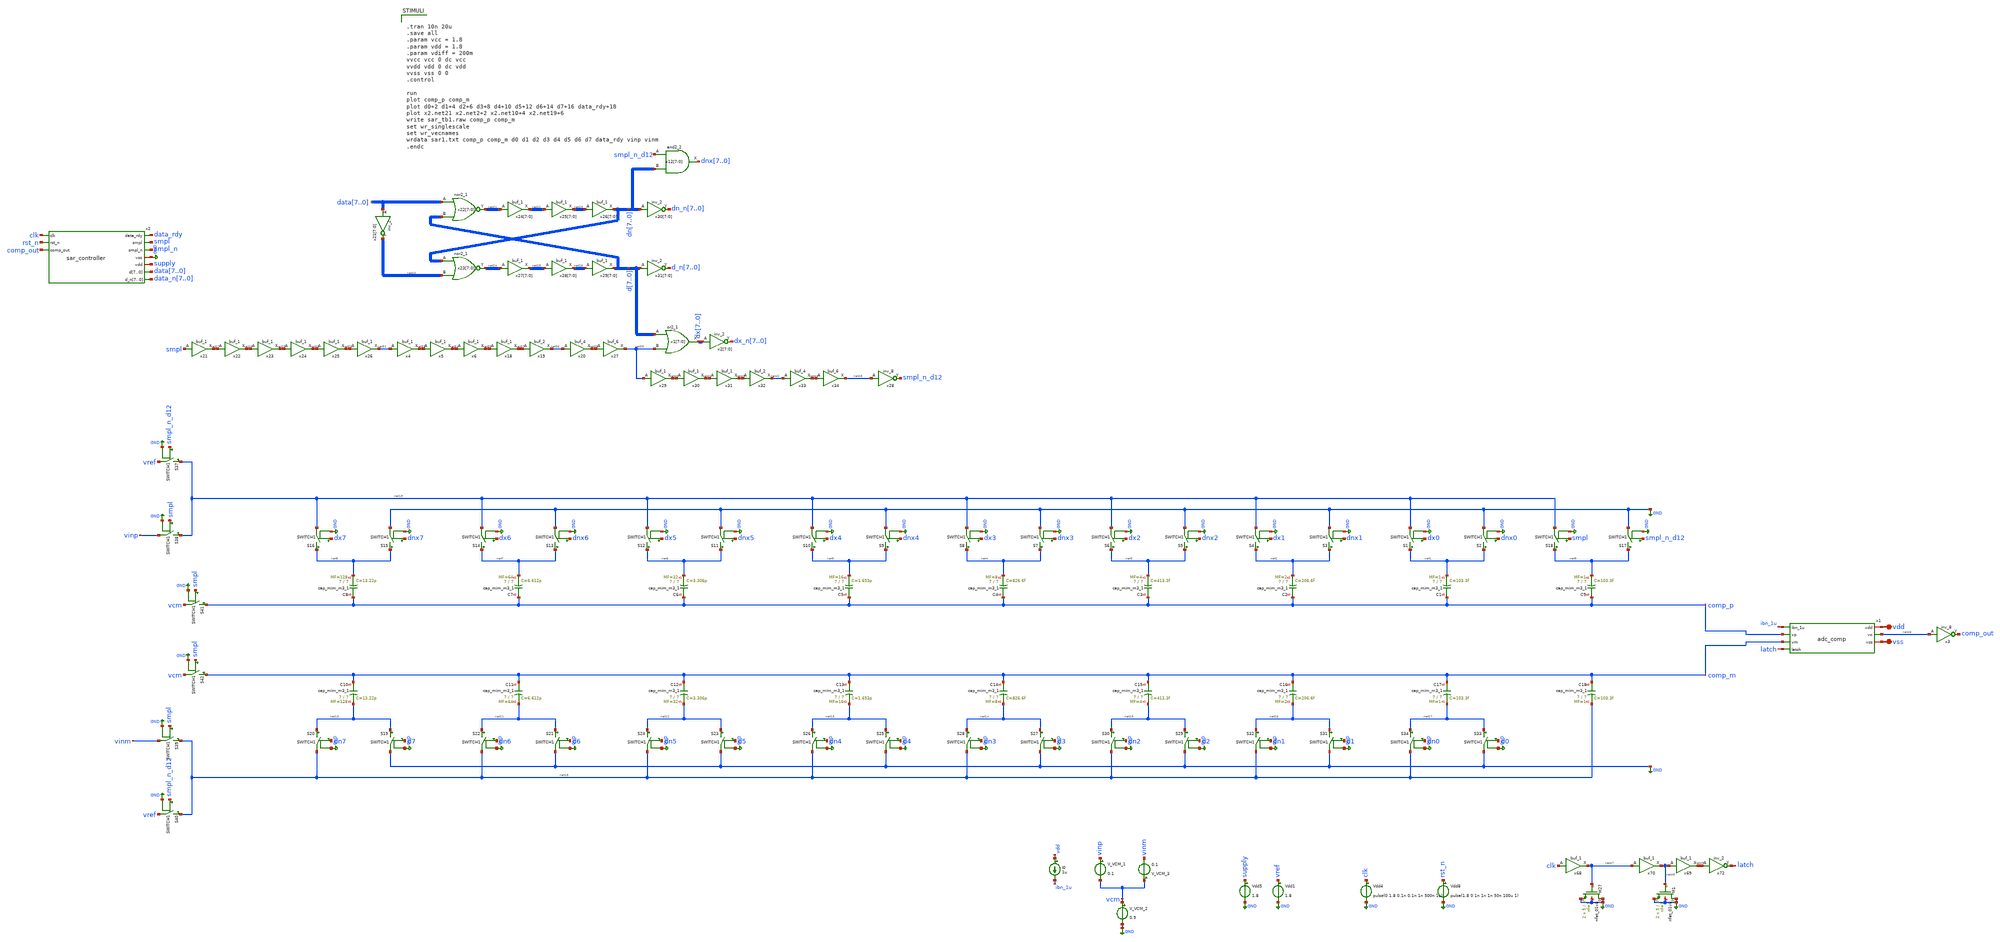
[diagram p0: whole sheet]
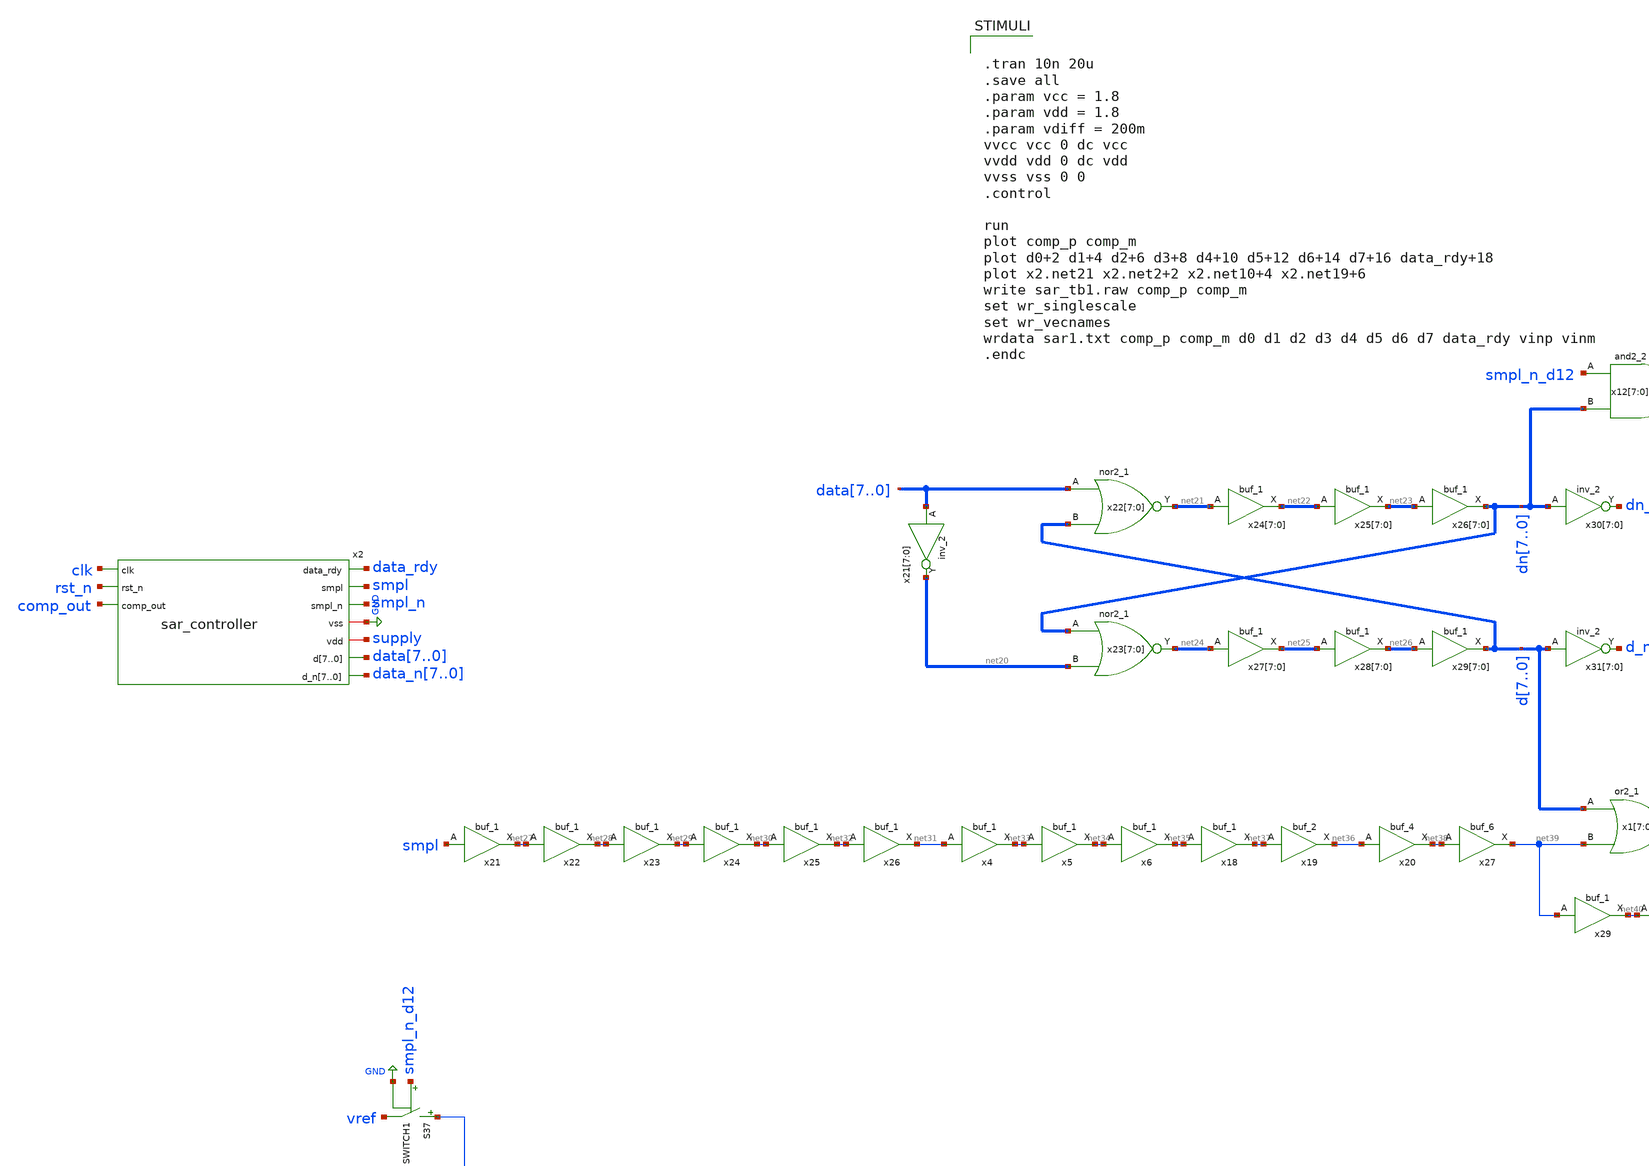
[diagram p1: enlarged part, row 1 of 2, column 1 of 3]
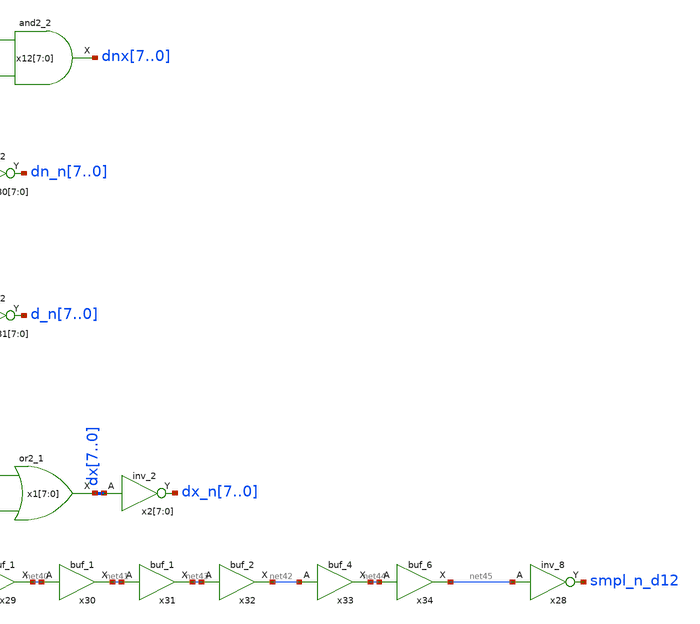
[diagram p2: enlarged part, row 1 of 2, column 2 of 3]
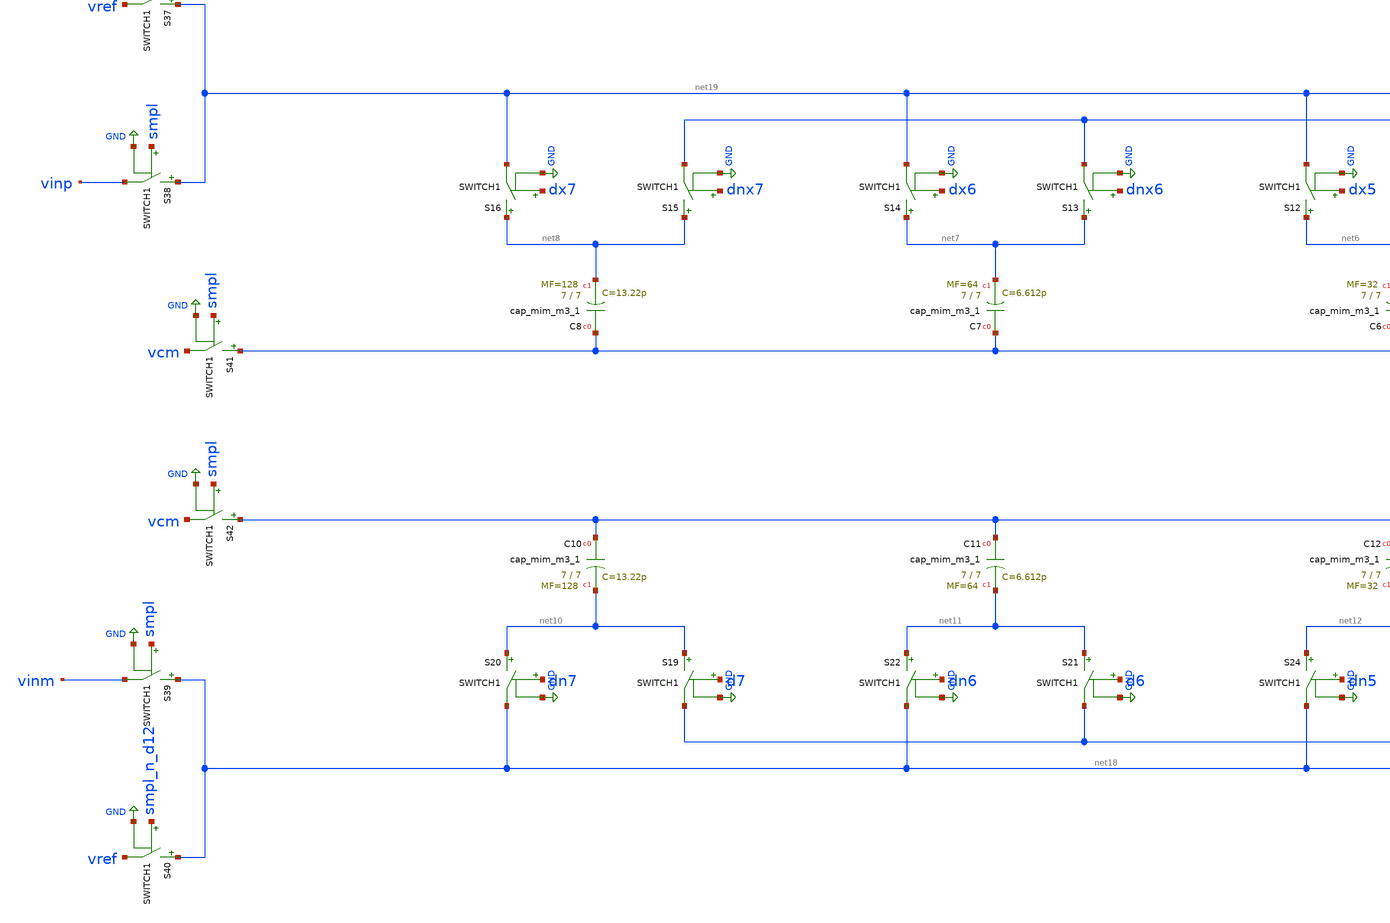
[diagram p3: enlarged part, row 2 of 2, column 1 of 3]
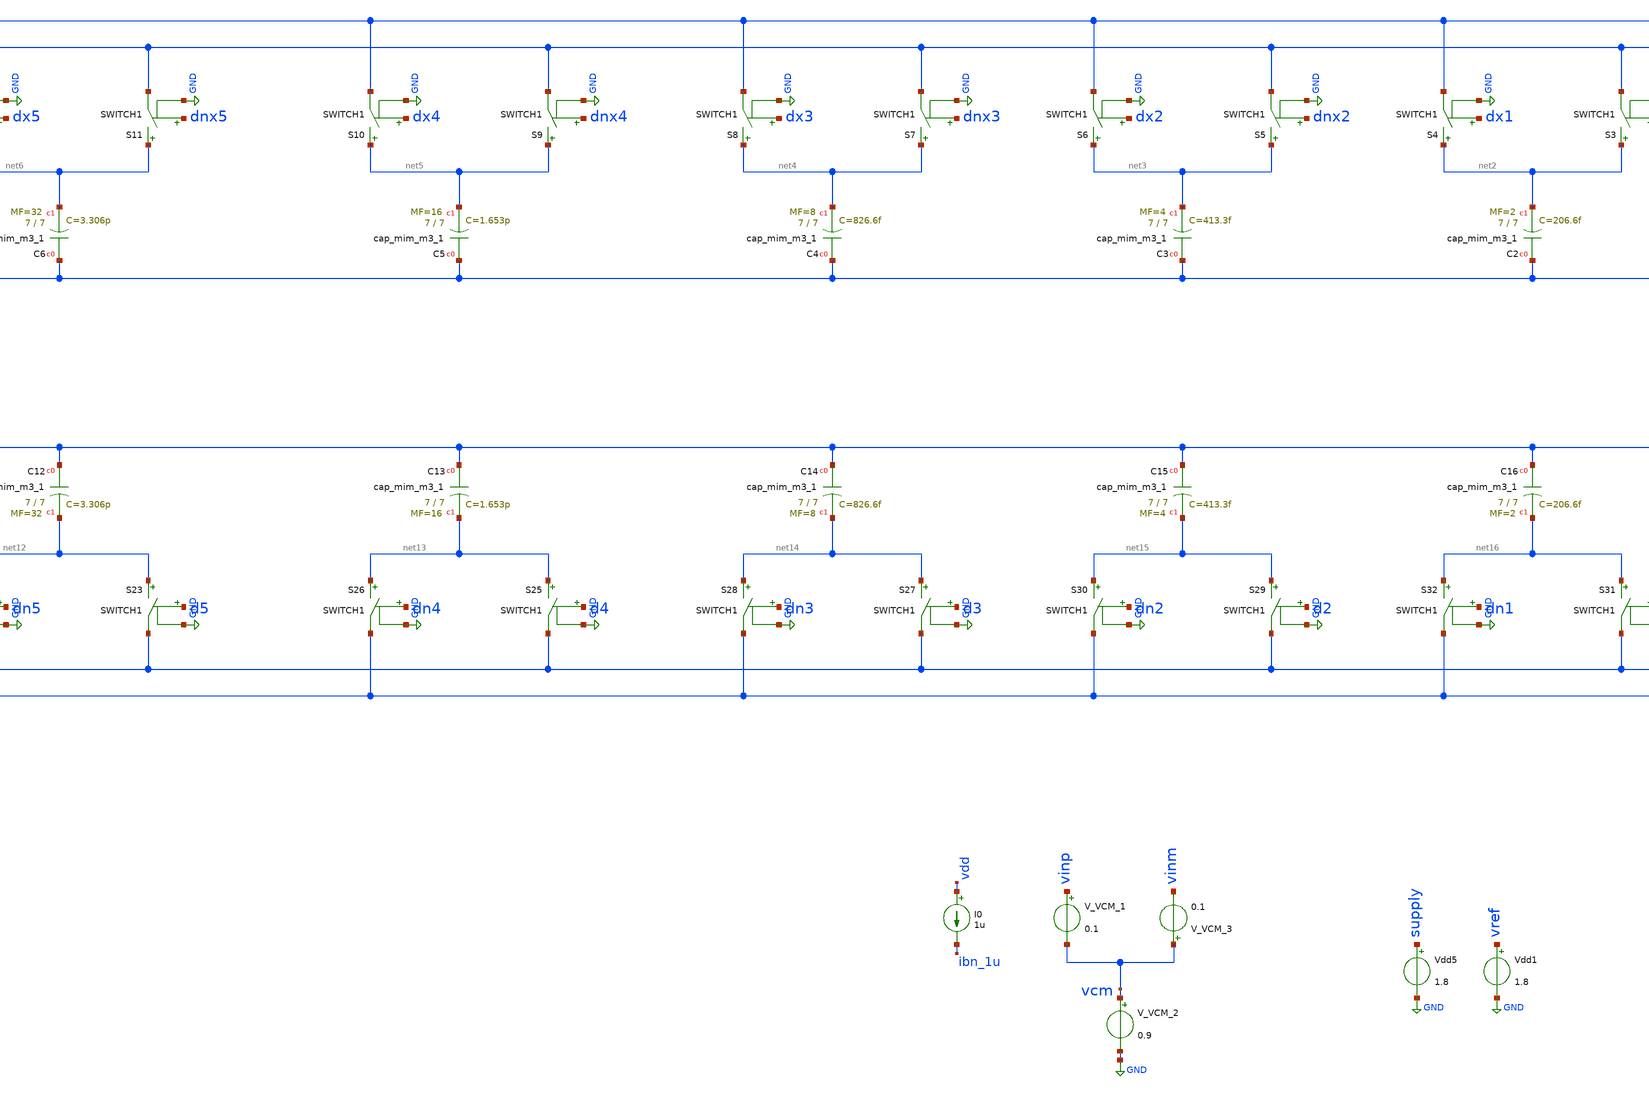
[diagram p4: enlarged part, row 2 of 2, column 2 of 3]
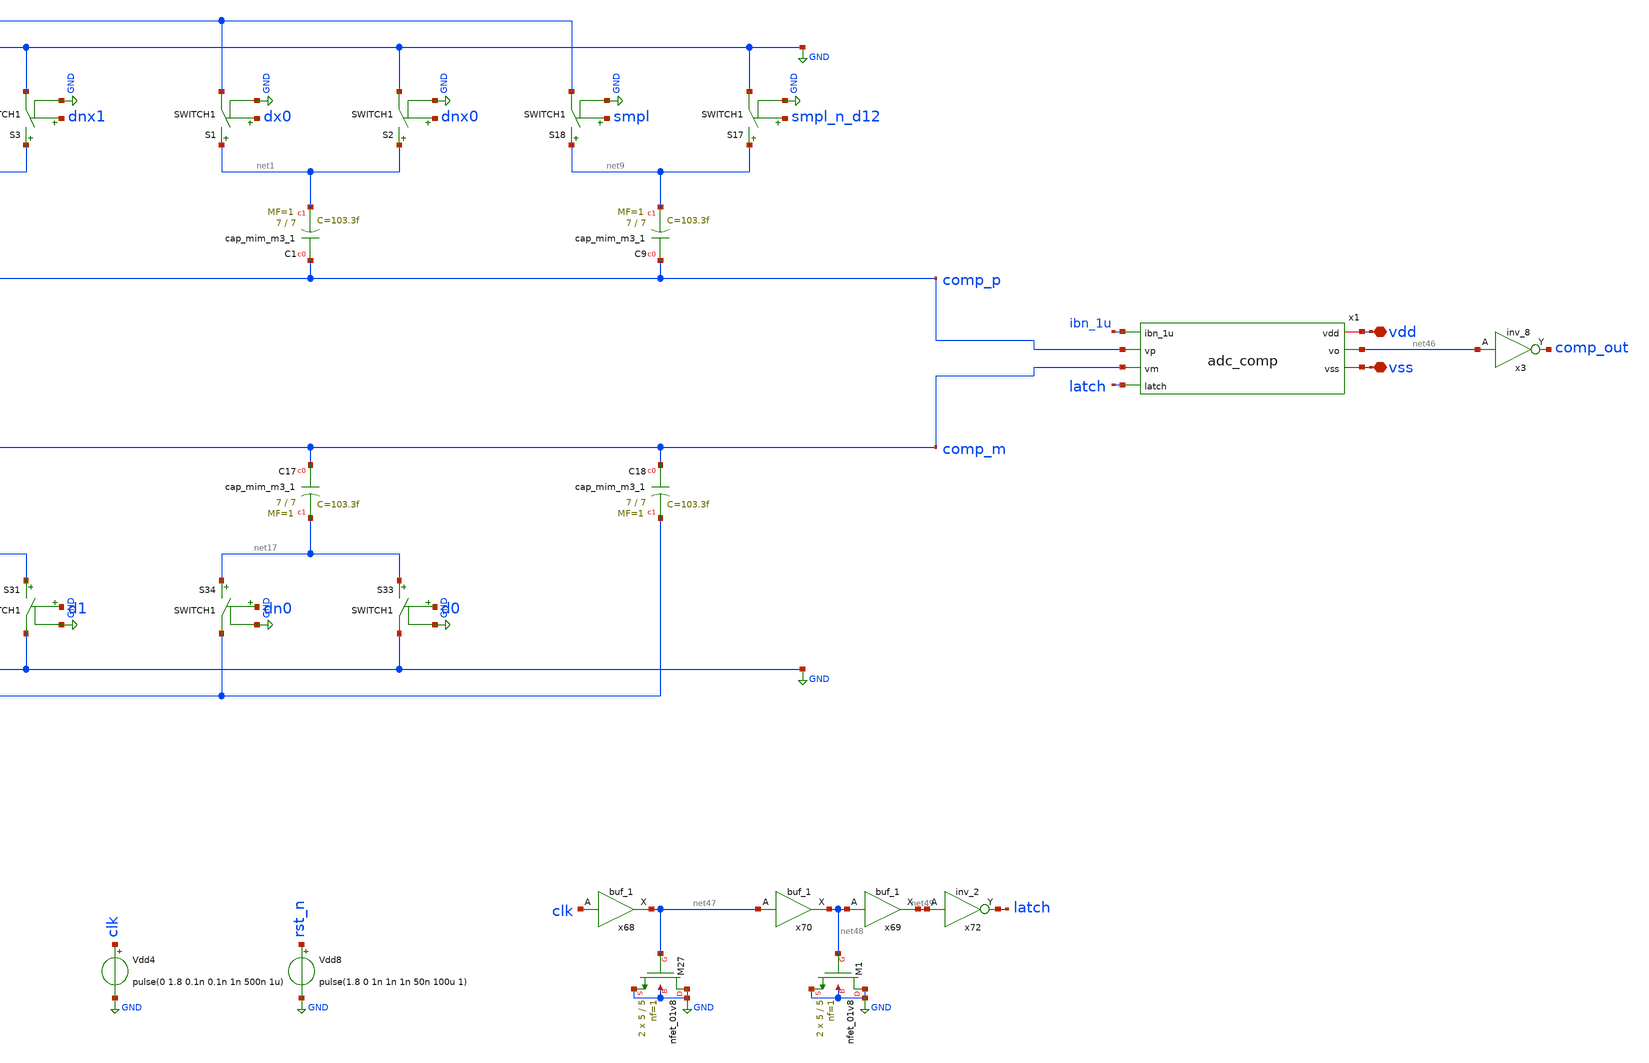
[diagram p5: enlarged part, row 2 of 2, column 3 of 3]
** sch_path: test/testbench/sar_tb1.sch
.lib $::SKYWATER_MODELS/sky130.lib.spice tt
.include $::SKYWATER_STDCELLS/sky130_fd_sc_hd.spice

**.subckt sar_tb1 vdd vss
*.iopin vdd
*.iopin vss
XC1 comp_p net1 sky130_fd_pr__cap_mim_m3_1 W=7 L=7 MF=1 m=1
S2 net1 GND dnx0 GND SWITCH1
S1 net1 net19 dx0 GND SWITCH1
XC2 comp_p net2 sky130_fd_pr__cap_mim_m3_1 W=7 L=7 MF=2 m=2
S3 net2 GND dnx1 GND SWITCH1
S4 net2 net19 dx1 GND SWITCH1
XC3 comp_p net3 sky130_fd_pr__cap_mim_m3_1 W=7 L=7 MF=4 m=4
S5 net3 GND dnx2 GND SWITCH1
S6 net3 net19 dx2 GND SWITCH1
XC4 comp_p net4 sky130_fd_pr__cap_mim_m3_1 W=7 L=7 MF=8 m=8
S7 net4 GND dnx3 GND SWITCH1
S8 net4 net19 dx3 GND SWITCH1
XC5 comp_p net5 sky130_fd_pr__cap_mim_m3_1 W=7 L=7 MF=16 m=16
S9 net5 GND dnx4 GND SWITCH1
S10 net5 net19 dx4 GND SWITCH1
XC6 comp_p net6 sky130_fd_pr__cap_mim_m3_1 W=7 L=7 MF=32 m=32
S11 net6 GND dnx5 GND SWITCH1
S12 net6 net19 dx5 GND SWITCH1
XC7 comp_p net7 sky130_fd_pr__cap_mim_m3_1 W=7 L=7 MF=64 m=64
S13 net7 GND dnx6 GND SWITCH1
S14 net7 net19 dx6 GND SWITCH1
S15 net8 GND dnx7 GND SWITCH1
S16 net8 net19 dx7 GND SWITCH1
XC9 comp_p net9 sky130_fd_pr__cap_mim_m3_1 W=7 L=7 MF=1 m=1
S17 net9 GND smpl_n_d12 GND SWITCH1
S18 net9 net19 smpl GND SWITCH1
XC10 comp_m net10 sky130_fd_pr__cap_mim_m3_1 W=7 L=7 MF=128 m=128
S19 net10 GND d7 GND SWITCH1
S20 net10 net18 dn7 GND SWITCH1
XC11 comp_m net11 sky130_fd_pr__cap_mim_m3_1 W=7 L=7 MF=64 m=64
S21 net11 GND d6 GND SWITCH1
S22 net11 net18 dn6 GND SWITCH1
XC12 comp_m net12 sky130_fd_pr__cap_mim_m3_1 W=7 L=7 MF=32 m=32
S23 net12 GND d5 GND SWITCH1
S24 net12 net18 dn5 GND SWITCH1
XC13 comp_m net13 sky130_fd_pr__cap_mim_m3_1 W=7 L=7 MF=16 m=16
S25 net13 GND d4 GND SWITCH1
S26 net13 net18 dn4 GND SWITCH1
XC14 comp_m net14 sky130_fd_pr__cap_mim_m3_1 W=7 L=7 MF=8 m=8
S27 net14 GND d3 GND SWITCH1
S28 net14 net18 dn3 GND SWITCH1
XC15 comp_m net15 sky130_fd_pr__cap_mim_m3_1 W=7 L=7 MF=4 m=4
S29 net15 GND d2 GND SWITCH1
S30 net15 net18 dn2 GND SWITCH1
XC16 comp_m net16 sky130_fd_pr__cap_mim_m3_1 W=7 L=7 MF=2 m=2
S31 net16 GND d1 GND SWITCH1
S32 net16 net18 dn1 GND SWITCH1
XC17 comp_m net17 sky130_fd_pr__cap_mim_m3_1 W=7 L=7 MF=1 m=1
S33 net17 GND d0 GND SWITCH1
S34 net17 net18 dn0 GND SWITCH1
XC18 comp_m net18 sky130_fd_pr__cap_mim_m3_1 W=7 L=7 MF=1 m=1
S37 net19 vref smpl_n_d12 GND SWITCH1
S39 net18 vinm smpl GND SWITCH1
S40 net18 vref smpl_n_d12 GND SWITCH1
S41 comp_p vcm smpl GND SWITCH1
S42 comp_m vcm smpl GND SWITCH1
Vdd8 rst_n GND pulse(1.8 0 1n 1n 1n 50n 100u 1)
Vdd4 clk GND pulse(0 1.8 0.1n 0.1n 1n 500n 1u)
Vdd1 vref GND 1.8
S38 net19 vinp smpl GND SWITCH1
XC8 comp_p net8 sky130_fd_pr__cap_mim_m3_1 W=7 L=7 MF=128 m=128
x3 net46 vss vss vcc vcc comp_out sky130_fd_sc_hd__inv_8
x2 clk data_rdy smpl rst_n smpl_n comp_out GND supply data7 data6 data5 data4 data3 data2 data1
+ data0 data_n7 data_n6 data_n5 data_n4 data_n3 data_n2 data_n1 data_n0 sar_controller
Vdd5 supply GND 1.8
V_VCM_2 vcm GND 0.9
V_VCM_1 vinp vcm 0.1
V_VCM_3 vcm vinm 0.1
x21[7] data7 vss vss vcc vcc net20[7] sky130_fd_sc_hd__inv_2
x21[6] data6 vss vss vcc vcc net20[6] sky130_fd_sc_hd__inv_2
x21[5] data5 vss vss vcc vcc net20[5] sky130_fd_sc_hd__inv_2
x21[4] data4 vss vss vcc vcc net20[4] sky130_fd_sc_hd__inv_2
x21[3] data3 vss vss vcc vcc net20[3] sky130_fd_sc_hd__inv_2
x21[2] data2 vss vss vcc vcc net20[2] sky130_fd_sc_hd__inv_2
x21[1] data1 vss vss vcc vcc net20[1] sky130_fd_sc_hd__inv_2
x21[0] data0 vss vss vcc vcc net20[0] sky130_fd_sc_hd__inv_2
x22[7] data7 d7 vss vss vdd vdd net21[7] sky130_fd_sc_hd__nor2_1
x22[6] data6 d6 vss vss vdd vdd net21[6] sky130_fd_sc_hd__nor2_1
x22[5] data5 d5 vss vss vdd vdd net21[5] sky130_fd_sc_hd__nor2_1
x22[4] data4 d4 vss vss vdd vdd net21[4] sky130_fd_sc_hd__nor2_1
x22[3] data3 d3 vss vss vdd vdd net21[3] sky130_fd_sc_hd__nor2_1
x22[2] data2 d2 vss vss vdd vdd net21[2] sky130_fd_sc_hd__nor2_1
x22[1] data1 d1 vss vss vdd vdd net21[1] sky130_fd_sc_hd__nor2_1
x22[0] data0 d0 vss vss vdd vdd net21[0] sky130_fd_sc_hd__nor2_1
x23[7] dn7 net20[7] vss vss vdd vdd net24[7] sky130_fd_sc_hd__nor2_1
x23[6] dn6 net20[6] vss vss vdd vdd net24[6] sky130_fd_sc_hd__nor2_1
x23[5] dn5 net20[5] vss vss vdd vdd net24[5] sky130_fd_sc_hd__nor2_1
x23[4] dn4 net20[4] vss vss vdd vdd net24[4] sky130_fd_sc_hd__nor2_1
x23[3] dn3 net20[3] vss vss vdd vdd net24[3] sky130_fd_sc_hd__nor2_1
x23[2] dn2 net20[2] vss vss vdd vdd net24[2] sky130_fd_sc_hd__nor2_1
x23[1] dn1 net20[1] vss vss vdd vdd net24[1] sky130_fd_sc_hd__nor2_1
x23[0] dn0 net20[0] vss vss vdd vdd net24[0] sky130_fd_sc_hd__nor2_1
x24[7] net21[7] vss vss vdd vdd net22[7] sky130_fd_sc_hd__buf_1
x24[6] net21[6] vss vss vdd vdd net22[6] sky130_fd_sc_hd__buf_1
x24[5] net21[5] vss vss vdd vdd net22[5] sky130_fd_sc_hd__buf_1
x24[4] net21[4] vss vss vdd vdd net22[4] sky130_fd_sc_hd__buf_1
x24[3] net21[3] vss vss vdd vdd net22[3] sky130_fd_sc_hd__buf_1
x24[2] net21[2] vss vss vdd vdd net22[2] sky130_fd_sc_hd__buf_1
x24[1] net21[1] vss vss vdd vdd net22[1] sky130_fd_sc_hd__buf_1
x24[0] net21[0] vss vss vdd vdd net22[0] sky130_fd_sc_hd__buf_1
x25[7] net22[7] vss vss vdd vdd net23[7] sky130_fd_sc_hd__buf_1
x25[6] net22[6] vss vss vdd vdd net23[6] sky130_fd_sc_hd__buf_1
x25[5] net22[5] vss vss vdd vdd net23[5] sky130_fd_sc_hd__buf_1
x25[4] net22[4] vss vss vdd vdd net23[4] sky130_fd_sc_hd__buf_1
x25[3] net22[3] vss vss vdd vdd net23[3] sky130_fd_sc_hd__buf_1
x25[2] net22[2] vss vss vdd vdd net23[2] sky130_fd_sc_hd__buf_1
x25[1] net22[1] vss vss vdd vdd net23[1] sky130_fd_sc_hd__buf_1
x25[0] net22[0] vss vss vdd vdd net23[0] sky130_fd_sc_hd__buf_1
x26[7] net23[7] vss vss vdd vdd dn7 sky130_fd_sc_hd__buf_1
x26[6] net23[6] vss vss vdd vdd dn6 sky130_fd_sc_hd__buf_1
x26[5] net23[5] vss vss vdd vdd dn5 sky130_fd_sc_hd__buf_1
x26[4] net23[4] vss vss vdd vdd dn4 sky130_fd_sc_hd__buf_1
x26[3] net23[3] vss vss vdd vdd dn3 sky130_fd_sc_hd__buf_1
x26[2] net23[2] vss vss vdd vdd dn2 sky130_fd_sc_hd__buf_1
x26[1] net23[1] vss vss vdd vdd dn1 sky130_fd_sc_hd__buf_1
x26[0] net23[0] vss vss vdd vdd dn0 sky130_fd_sc_hd__buf_1
x27[7] net24[7] vss vss vdd vdd net25[7] sky130_fd_sc_hd__buf_1
x27[6] net24[6] vss vss vdd vdd net25[6] sky130_fd_sc_hd__buf_1
x27[5] net24[5] vss vss vdd vdd net25[5] sky130_fd_sc_hd__buf_1
x27[4] net24[4] vss vss vdd vdd net25[4] sky130_fd_sc_hd__buf_1
x27[3] net24[3] vss vss vdd vdd net25[3] sky130_fd_sc_hd__buf_1
x27[2] net24[2] vss vss vdd vdd net25[2] sky130_fd_sc_hd__buf_1
x27[1] net24[1] vss vss vdd vdd net25[1] sky130_fd_sc_hd__buf_1
x27[0] net24[0] vss vss vdd vdd net25[0] sky130_fd_sc_hd__buf_1
x28[7] net25[7] vss vss vdd vdd net26[7] sky130_fd_sc_hd__buf_1
x28[6] net25[6] vss vss vdd vdd net26[6] sky130_fd_sc_hd__buf_1
x28[5] net25[5] vss vss vdd vdd net26[5] sky130_fd_sc_hd__buf_1
x28[4] net25[4] vss vss vdd vdd net26[4] sky130_fd_sc_hd__buf_1
x28[3] net25[3] vss vss vdd vdd net26[3] sky130_fd_sc_hd__buf_1
x28[2] net25[2] vss vss vdd vdd net26[2] sky130_fd_sc_hd__buf_1
x28[1] net25[1] vss vss vdd vdd net26[1] sky130_fd_sc_hd__buf_1
x28[0] net25[0] vss vss vdd vdd net26[0] sky130_fd_sc_hd__buf_1
x29[7] net26[7] vss vss vdd vdd d7 sky130_fd_sc_hd__buf_1
x29[6] net26[6] vss vss vdd vdd d6 sky130_fd_sc_hd__buf_1
x29[5] net26[5] vss vss vdd vdd d5 sky130_fd_sc_hd__buf_1
x29[4] net26[4] vss vss vdd vdd d4 sky130_fd_sc_hd__buf_1
x29[3] net26[3] vss vss vdd vdd d3 sky130_fd_sc_hd__buf_1
x29[2] net26[2] vss vss vdd vdd d2 sky130_fd_sc_hd__buf_1
x29[1] net26[1] vss vss vdd vdd d1 sky130_fd_sc_hd__buf_1
x29[0] net26[0] vss vss vdd vdd d0 sky130_fd_sc_hd__buf_1
x30[7] dn7 vss vss vcc vcc dn_n7 sky130_fd_sc_hd__inv_2
x30[6] dn6 vss vss vcc vcc dn_n6 sky130_fd_sc_hd__inv_2
x30[5] dn5 vss vss vcc vcc dn_n5 sky130_fd_sc_hd__inv_2
x30[4] dn4 vss vss vcc vcc dn_n4 sky130_fd_sc_hd__inv_2
x30[3] dn3 vss vss vcc vcc dn_n3 sky130_fd_sc_hd__inv_2
x30[2] dn2 vss vss vcc vcc dn_n2 sky130_fd_sc_hd__inv_2
x30[1] dn1 vss vss vcc vcc dn_n1 sky130_fd_sc_hd__inv_2
x30[0] dn0 vss vss vcc vcc dn_n0 sky130_fd_sc_hd__inv_2
x31[7] d7 vss vss vcc vcc d_n7 sky130_fd_sc_hd__inv_2
x31[6] d6 vss vss vcc vcc d_n6 sky130_fd_sc_hd__inv_2
x31[5] d5 vss vss vcc vcc d_n5 sky130_fd_sc_hd__inv_2
x31[4] d4 vss vss vcc vcc d_n4 sky130_fd_sc_hd__inv_2
x31[3] d3 vss vss vcc vcc d_n3 sky130_fd_sc_hd__inv_2
x31[2] d2 vss vss vcc vcc d_n2 sky130_fd_sc_hd__inv_2
x31[1] d1 vss vss vcc vcc d_n1 sky130_fd_sc_hd__inv_2
x31[0] d0 vss vss vcc vcc d_n0 sky130_fd_sc_hd__inv_2
x1[7] d7 net39 vss vss vcc vcc dx7 sky130_fd_sc_hd__or2_1
x1[6] d6 net39 vss vss vcc vcc dx6 sky130_fd_sc_hd__or2_1
x1[5] d5 net39 vss vss vcc vcc dx5 sky130_fd_sc_hd__or2_1
x1[4] d4 net39 vss vss vcc vcc dx4 sky130_fd_sc_hd__or2_1
x1[3] d3 net39 vss vss vcc vcc dx3 sky130_fd_sc_hd__or2_1
x1[2] d2 net39 vss vss vcc vcc dx2 sky130_fd_sc_hd__or2_1
x1[1] d1 net39 vss vss vcc vcc dx1 sky130_fd_sc_hd__or2_1
x1[0] d0 net39 vss vss vcc vcc dx0 sky130_fd_sc_hd__or2_1
x21 smpl vss vss vdd vdd net27 sky130_fd_sc_hd__buf_1
x22 net27 vss vss vdd vdd net28 sky130_fd_sc_hd__buf_1
x23 net28 vss vss vdd vdd net29 sky130_fd_sc_hd__buf_1
x24 net29 vss vss vdd vdd net30 sky130_fd_sc_hd__buf_1
x25 net30 vss vss vdd vdd net32 sky130_fd_sc_hd__buf_1
x26 net32 vss vss vdd vdd net31 sky130_fd_sc_hd__buf_1
x2[7] dx7 vss vss vcc vcc dx_n7 sky130_fd_sc_hd__inv_2
x2[6] dx6 vss vss vcc vcc dx_n6 sky130_fd_sc_hd__inv_2
x2[5] dx5 vss vss vcc vcc dx_n5 sky130_fd_sc_hd__inv_2
x2[4] dx4 vss vss vcc vcc dx_n4 sky130_fd_sc_hd__inv_2
x2[3] dx3 vss vss vcc vcc dx_n3 sky130_fd_sc_hd__inv_2
x2[2] dx2 vss vss vcc vcc dx_n2 sky130_fd_sc_hd__inv_2
x2[1] dx1 vss vss vcc vcc dx_n1 sky130_fd_sc_hd__inv_2
x2[0] dx0 vss vss vcc vcc dx_n0 sky130_fd_sc_hd__inv_2
x12[7] smpl_n_d12 dn7 vss vss vcc vcc dnx7 sky130_fd_sc_hd__and2_2
x12[6] smpl_n_d12 dn6 vss vss vcc vcc dnx6 sky130_fd_sc_hd__and2_2
x12[5] smpl_n_d12 dn5 vss vss vcc vcc dnx5 sky130_fd_sc_hd__and2_2
x12[4] smpl_n_d12 dn4 vss vss vcc vcc dnx4 sky130_fd_sc_hd__and2_2
x12[3] smpl_n_d12 dn3 vss vss vcc vcc dnx3 sky130_fd_sc_hd__and2_2
x12[2] smpl_n_d12 dn2 vss vss vcc vcc dnx2 sky130_fd_sc_hd__and2_2
x12[1] smpl_n_d12 dn1 vss vss vcc vcc dnx1 sky130_fd_sc_hd__and2_2
x12[0] smpl_n_d12 dn0 vss vss vcc vcc dnx0 sky130_fd_sc_hd__and2_2
x4 net31 vss vss vdd vdd net33 sky130_fd_sc_hd__buf_1
x5 net33 vss vss vdd vdd net34 sky130_fd_sc_hd__buf_1
x6 net34 vss vss vdd vdd net35 sky130_fd_sc_hd__buf_1
x18 net35 vss vss vdd vdd net37 sky130_fd_sc_hd__buf_1
x19 net37 vss vss vdd vdd net36 sky130_fd_sc_hd__buf_2
x20 net36 vss vss vdd vdd net38 sky130_fd_sc_hd__buf_4
x27 net38 vss vss vdd vdd net39 sky130_fd_sc_hd__buf_6
x28 net45 vss vss vcc vcc smpl_n_d12 sky130_fd_sc_hd__inv_8
x29 net39 vss vss vdd vdd net40 sky130_fd_sc_hd__buf_1
x30 net40 vss vss vdd vdd net41 sky130_fd_sc_hd__buf_1
x31 net41 vss vss vdd vdd net43 sky130_fd_sc_hd__buf_1
x32 net43 vss vss vdd vdd net42 sky130_fd_sc_hd__buf_2
x33 net42 vss vss vdd vdd net44 sky130_fd_sc_hd__buf_4
x34 net44 vss vss vdd vdd net45 sky130_fd_sc_hd__buf_6
x1 vdd net46 ibn_1u comp_p comp_m vss latch adc_comp
I0 vdd ibn_1u 1u
x68 clk vss vss vdd vdd net47 sky130_fd_sc_hd__buf_1
x70 net47 vss vss vdd vdd net48 sky130_fd_sc_hd__buf_1
x72 net49 vss vss vcc vcc latch sky130_fd_sc_hd__inv_2
XM27 GND net47 GND GND sky130_fd_pr__nfet_01v8 L=5 W=5 nf=1 ad='int((nf+1)/2) * W/nf * 0.29' as='int((nf+2)/2) * W/nf * 0.29'
+ pd='2*int((nf+1)/2) * (W/nf + 0.29)' ps='2*int((nf+2)/2) * (W/nf + 0.29)' nrd='0.29 / W' nrs='0.29 / W'
+ sa=0 sb=0 sd=0 mult=2 m=2
XM1 GND net48 GND GND sky130_fd_pr__nfet_01v8 L=5 W=5 nf=1 ad='int((nf+1)/2) * W/nf * 0.29' as='int((nf+2)/2) * W/nf * 0.29'
+ pd='2*int((nf+1)/2) * (W/nf + 0.29)' ps='2*int((nf+2)/2) * (W/nf + 0.29)' nrd='0.29 / W' nrs='0.29 / W'
+ sa=0 sb=0 sd=0 mult=2 m=2
x69 net48 vss vss vdd vdd net49 sky130_fd_sc_hd__buf_1
**** begin user architecture code


.tran 10n 20u
.save all
.param vcc = 1.8
.param vdd = 1.8
.param vdiff = 200m
vvcc vcc 0 dc vcc
vvdd vdd 0 dc vdd
vvss vss 0 0
.control

run
plot comp_p comp_m
plot d0+2 d1+4 d2+6 d3+8 d4+10 d5+12 d6+14 d7+16 data_rdy+18
plot x2.net21 x2.net2+2 x2.net10+4 x2.net19+6
write sar_tb1.raw comp_p comp_m
set wr_singlescale
set wr_vecnames
wrdata sar1.txt comp_p comp_m d0 d1 d2 d3 d4 d5 d6 d7 data_rdy vinp vinm
.endc



.model SWITCH1 sw vt=0.9 vh=0 ron=1 roff =100G

**** end user architecture code
**.ends

* expanding   symbol:  /foss/designs/test/design/sar_controller.sym # of pins=10
** sym_path: test/design/sar_controller.sym
** sch_path: test/design/sar_controller.sch
.subckt sar_controller clk data_rdy smpl rst_n smpl_n comp_out vss vdd d7 d6 d5 d4 d3 d2 d1 d0 d_n7
+ d_n6 d_n5 d_n4 d_n3 d_n2 d_n1 d_n0
*.ipin rst_n
*.opin data_rdy
*.ipin clk
*.opin smpl
*.ipin comp_out
*.iopin vss
*.iopin vdd
*.opin d7,d6,d5,d4,d3,d2,d1,d0
*.opin d_n7,d_n6,d_n5,d_n4,d_n3,d_n2,d_n1,d_n0
*.opin smpl_n
x26 net2 net21 net22 net9 vss vss vdd vdd net1 net25 sky130_fd_sc_hd__dfbbp_1
x5 net19 net23 net20 vss vss vdd vdd cnv_7 net9 sky130_fd_sc_hd__dfrbp_1
* noconn #net33
x24 net19 net8 net20 vss vss vdd vdd net23 net24 sky130_fd_sc_hd__dfsbp_1
x6 net24 net20 vss vss vdd vdd net22 sky130_fd_sc_hd__and2_4
x1 net19 cnv_7 net20 vss vss vdd vdd cnv_6 net12 sky130_fd_sc_hd__dfrbp_1
x2 net19 cnv_6 net20 vss vss vdd vdd cnv_5 net13 sky130_fd_sc_hd__dfrbp_1
x3 net19 cnv_5 net20 vss vss vdd vdd cnv_4 net14 sky130_fd_sc_hd__dfrbp_1
x4 net19 cnv_4 net20 vss vss vdd vdd cnv_3 net15 sky130_fd_sc_hd__dfrbp_1
x7 net19 cnv_3 net20 vss vss vdd vdd cnv_2 net16 sky130_fd_sc_hd__dfrbp_1
x8 net19 cnv_2 net20 vss vss vdd vdd cnv_1 net17 sky130_fd_sc_hd__dfrbp_1
x9 net19 cnv_1 net20 vss vss vdd vdd cnv_0 net18 sky130_fd_sc_hd__dfrbp_1
x10 net19 cnv_0 net20 vss vss vdd vdd net8 net33 sky130_fd_sc_hd__dfrbp_1
x11 vss vss net22 vss vss vdd vdd net11 net34 sky130_fd_sc_hd__dfrbp_1
x12 net10 net21 net22 net12 vss vss vdd vdd net2 net26 sky130_fd_sc_hd__dfbbp_1
x13 net3 net21 net22 net13 vss vss vdd vdd net10 net27 sky130_fd_sc_hd__dfbbp_1
x14 net4 net21 net22 net14 vss vss vdd vdd net3 net28 sky130_fd_sc_hd__dfbbp_1
x15 net5 net21 net22 net15 vss vss vdd vdd net4 net29 sky130_fd_sc_hd__dfbbp_1
x16 net6 net21 net22 net16 vss vss vdd vdd net5 net30 sky130_fd_sc_hd__dfbbp_1
x17 net7 net21 net22 net17 vss vss vdd vdd net6 net31 sky130_fd_sc_hd__dfbbp_1
x18 net11 net21 net22 net18 vss vss vdd vdd net7 net32 sky130_fd_sc_hd__dfbbp_1
* noconn #net34
x19 net1 vss vss vdd vdd d7 sky130_fd_sc_hd__buf_2
x20 net25 vss vss vdd vdd d_n7 sky130_fd_sc_hd__buf_2
x21 net2 vss vss vdd vdd d6 sky130_fd_sc_hd__buf_2
x22 net26 vss vss vdd vdd d_n6 sky130_fd_sc_hd__buf_2
x23 net10 vss vss vdd vdd d5 sky130_fd_sc_hd__buf_2
x25 net27 vss vss vdd vdd d_n5 sky130_fd_sc_hd__buf_2
x27 net3 vss vss vdd vdd d4 sky130_fd_sc_hd__buf_2
x28 net28 vss vss vdd vdd d_n4 sky130_fd_sc_hd__buf_2
x29 net4 vss vss vdd vdd d3 sky130_fd_sc_hd__buf_2
x30 net29 vss vss vdd vdd d_n3 sky130_fd_sc_hd__buf_2
x31 net5 vss vss vdd vdd d2 sky130_fd_sc_hd__buf_2
x32 net30 vss vss vdd vdd d_n2 sky130_fd_sc_hd__buf_2
x33 net6 vss vss vdd vdd d1 sky130_fd_sc_hd__buf_2
x34 net31 vss vss vdd vdd d_n1 sky130_fd_sc_hd__buf_2
x35 net7 vss vss vdd vdd d0 sky130_fd_sc_hd__buf_2
x36 net32 vss vss vdd vdd d_n0 sky130_fd_sc_hd__buf_2
x37 net23 vss vss vdd vdd smpl sky130_fd_sc_hd__buf_2
x38 net24 vss vss vdd vdd smpl_n sky130_fd_sc_hd__buf_2
x39 net8 vss vss vdd vdd data_rdy sky130_fd_sc_hd__buf_2
x40 comp_out vss vss vdd vdd net21 sky130_fd_sc_hd__buf_4
x41 rst_n vss vss vdd vdd net20 sky130_fd_sc_hd__buf_4
x42 clk vss vss vdd vdd net19 sky130_fd_sc_hd__buf_4
.ends


* expanding   symbol:  /foss/designs/test/design/adc_comp.sym # of pins=7
** sym_path: test/design/adc_comp.sym
** sch_path: test/design/adc_comp.sch
.subckt adc_comp vdd vo ibn_1u vp vm vss latch
*.iopin vss
*.iopin vdd
*.ipin vp
*.ipin vm
*.ipin latch
*.ipin ibn_1u
*.opin vo
XM3 vom1 vp vx vss sky130_fd_pr__nfet_01v8_lvt L=1 W=2 nf=1 ad='int((nf+1)/2) * W/nf * 0.29' as='int((nf+2)/2) * W/nf * 0.29'
+ pd='2*int((nf+1)/2) * (W/nf + 0.29)' ps='2*int((nf+2)/2) * (W/nf + 0.29)' nrd='0.29 / W' nrs='0.29 / W'
+ sa=0 sb=0 sd=0 mult=8 m=8
XM4 vop1 vm vx vss sky130_fd_pr__nfet_01v8_lvt L=1 W=2 nf=1 ad='int((nf+1)/2) * W/nf * 0.29' as='int((nf+2)/2) * W/nf * 0.29'
+ pd='2*int((nf+1)/2) * (W/nf + 0.29)' ps='2*int((nf+2)/2) * (W/nf + 0.29)' nrd='0.29 / W' nrs='0.29 / W'
+ sa=0 sb=0 sd=0 mult=8 m=8
XM2 vop1 vbp vdd vdd sky130_fd_pr__pfet_01v8_lvt L=5 W=5 nf=1 ad='int((nf+1)/2) * W/nf * 0.29' as='int((nf+2)/2) * W/nf * 0.29'
+ pd='2*int((nf+1)/2) * (W/nf + 0.29)' ps='2*int((nf+2)/2) * (W/nf + 0.29)' nrd='0.29 / W' nrs='0.29 / W'
+ sa=0 sb=0 sd=0 mult=5 m=5
XM1 vom1 vbp vdd vdd sky130_fd_pr__pfet_01v8_lvt L=5 W=5 nf=1 ad='int((nf+1)/2) * W/nf * 0.29' as='int((nf+2)/2) * W/nf * 0.29'
+ pd='2*int((nf+1)/2) * (W/nf + 0.29)' ps='2*int((nf+2)/2) * (W/nf + 0.29)' nrd='0.29 / W' nrs='0.29 / W'
+ sa=0 sb=0 sd=0 mult=5 m=5
XM6 ibn_1u ibn_1u vss vss sky130_fd_pr__nfet_01v8 L=20 W=3 nf=1 ad='int((nf+1)/2) * W/nf * 0.29' as='int((nf+2)/2) * W/nf * 0.29'
+ pd='2*int((nf+1)/2) * (W/nf + 0.29)' ps='2*int((nf+2)/2) * (W/nf + 0.29)' nrd='0.29 / W' nrs='0.29 / W'
+ sa=0 sb=0 sd=0 mult=2 m=2
XM5 vx ibn_1u vss vss sky130_fd_pr__nfet_01v8 L=20 W=3 nf=1 ad='int((nf+1)/2) * W/nf * 0.29' as='int((nf+2)/2) * W/nf * 0.29'
+ pd='2*int((nf+1)/2) * (W/nf + 0.29)' ps='2*int((nf+2)/2) * (W/nf + 0.29)' nrd='0.29 / W' nrs='0.29 / W'
+ sa=0 sb=0 sd=0 mult=12 m=12
XM7 vbp ibn_1u vss vss sky130_fd_pr__nfet_01v8 L=20 W=3 nf=1 ad='int((nf+1)/2) * W/nf * 0.29' as='int((nf+2)/2) * W/nf * 0.29'
+ pd='2*int((nf+1)/2) * (W/nf + 0.29)' ps='2*int((nf+2)/2) * (W/nf + 0.29)' nrd='0.29 / W' nrs='0.29 / W'
+ sa=0 sb=0 sd=0 mult=1 m=1
XM8 vbp vbp vdd vdd sky130_fd_pr__pfet_01v8_lvt L=5 W=5 nf=1 ad='int((nf+1)/2) * W/nf * 0.29' as='int((nf+2)/2) * W/nf * 0.29'
+ pd='2*int((nf+1)/2) * (W/nf + 0.29)' ps='2*int((nf+2)/2) * (W/nf + 0.29)' nrd='0.29 / W' nrs='0.29 / W'
+ sa=0 sb=0 sd=0 mult=1 m=1
XM9 vx vop1 vdd vdd sky130_fd_pr__pfet_01v8_lvt L=1 W=5 nf=1 ad='int((nf+1)/2) * W/nf * 0.29' as='int((nf+2)/2) * W/nf * 0.29'
+ pd='2*int((nf+1)/2) * (W/nf + 0.29)' ps='2*int((nf+2)/2) * (W/nf + 0.29)' nrd='0.29 / W' nrs='0.29 / W'
+ sa=0 sb=0 sd=0 mult=2 m=2
XM10 vx vom1 vdd vdd sky130_fd_pr__pfet_01v8_lvt L=1 W=5 nf=1 ad='int((nf+1)/2) * W/nf * 0.29' as='int((nf+2)/2) * W/nf * 0.29'
+ pd='2*int((nf+1)/2) * (W/nf + 0.29)' ps='2*int((nf+2)/2) * (W/nf + 0.29)' nrd='0.29 / W' nrs='0.29 / W'
+ sa=0 sb=0 sd=0 mult=2 m=2
XM11 vop2 vom2 vss vss sky130_fd_pr__nfet_01v8 L=2 W=3 nf=1 ad='int((nf+1)/2) * W/nf * 0.29' as='int((nf+2)/2) * W/nf * 0.29'
+ pd='2*int((nf+1)/2) * (W/nf + 0.29)' ps='2*int((nf+2)/2) * (W/nf + 0.29)' nrd='0.29 / W' nrs='0.29 / W'
+ sa=0 sb=0 sd=0 mult=1 m=1
XM12 vom2 vop2 vss vss sky130_fd_pr__nfet_01v8 L=2 W=3 nf=1 ad='int((nf+1)/2) * W/nf * 0.29' as='int((nf+2)/2) * W/nf * 0.29'
+ pd='2*int((nf+1)/2) * (W/nf + 0.29)' ps='2*int((nf+2)/2) * (W/nf + 0.29)' nrd='0.29 / W' nrs='0.29 / W'
+ sa=0 sb=0 sd=0 mult=1 m=1
XM13 net4 vom1 vdd vdd sky130_fd_pr__pfet_01v8_lvt L=0.4 W=5 nf=1 ad='int((nf+1)/2) * W/nf * 0.29' as='int((nf+2)/2) * W/nf * 0.29'
+ pd='2*int((nf+1)/2) * (W/nf + 0.29)' ps='2*int((nf+2)/2) * (W/nf + 0.29)' nrd='0.29 / W' nrs='0.29 / W'
+ sa=0 sb=0 sd=0 mult=1 m=1
XM14 net3 vop1 vdd vdd sky130_fd_pr__pfet_01v8_lvt L=0.4 W=5 nf=1 ad='int((nf+1)/2) * W/nf * 0.29' as='int((nf+2)/2) * W/nf * 0.29'
+ pd='2*int((nf+1)/2) * (W/nf + 0.29)' ps='2*int((nf+2)/2) * (W/nf + 0.29)' nrd='0.29 / W' nrs='0.29 / W'
+ sa=0 sb=0 sd=0 mult=1 m=1
XM17 vom2 latch_n vss vss sky130_fd_pr__nfet_01v8 L=0.15 W=0.5 nf=1 ad='int((nf+1)/2) * W/nf * 0.29'
+ as='int((nf+2)/2) * W/nf * 0.29' pd='2*int((nf+1)/2) * (W/nf + 0.29)' ps='2*int((nf+2)/2) * (W/nf + 0.29)'
+ nrd='0.29 / W' nrs='0.29 / W' sa=0 sb=0 sd=0 mult=1 m=1
XM18 vop2 latch_n vss vss sky130_fd_pr__nfet_01v8 L=0.15 W=0.5 nf=1 ad='int((nf+1)/2) * W/nf * 0.29'
+ as='int((nf+2)/2) * W/nf * 0.29' pd='2*int((nf+1)/2) * (W/nf + 0.29)' ps='2*int((nf+2)/2) * (W/nf + 0.29)'
+ nrd='0.29 / W' nrs='0.29 / W' sa=0 sb=0 sd=0 mult=1 m=1
XM19 net1 vop2 vdd vdd sky130_fd_pr__pfet_01v8 L=0.15 W=1 nf=1 ad='int((nf+1)/2) * W/nf * 0.29' as='int((nf+2)/2) * W/nf * 0.29'
+ pd='2*int((nf+1)/2) * (W/nf + 0.29)' ps='2*int((nf+2)/2) * (W/nf + 0.29)' nrd='0.29 / W' nrs='0.29 / W'
+ sa=0 sb=0 sd=0 mult=1 m=1
XM20 net1 vop2 vss vss sky130_fd_pr__nfet_01v8 L=0.15 W=0.5 nf=1 ad='int((nf+1)/2) * W/nf * 0.29' as='int((nf+2)/2) * W/nf * 0.29'
+ pd='2*int((nf+1)/2) * (W/nf + 0.29)' ps='2*int((nf+2)/2) * (W/nf + 0.29)' nrd='0.29 / W' nrs='0.29 / W'
+ sa=0 sb=0 sd=0 mult=1 m=1
XM21 vo net1 vdd vdd sky130_fd_pr__pfet_01v8 L=0.15 W=1 nf=1 ad='int((nf+1)/2) * W/nf * 0.29' as='int((nf+2)/2) * W/nf * 0.29'
+ pd='2*int((nf+1)/2) * (W/nf + 0.29)' ps='2*int((nf+2)/2) * (W/nf + 0.29)' nrd='0.29 / W' nrs='0.29 / W'
+ sa=0 sb=0 sd=0 mult=2 m=2
XM22 vo net1 vss vss sky130_fd_pr__nfet_01v8 L=0.15 W=0.5 nf=1 ad='int((nf+1)/2) * W/nf * 0.29' as='int((nf+2)/2) * W/nf * 0.29'
+ pd='2*int((nf+1)/2) * (W/nf + 0.29)' ps='2*int((nf+2)/2) * (W/nf + 0.29)' nrd='0.29 / W' nrs='0.29 / W'
+ sa=0 sb=0 sd=0 mult=2 m=2
XM23 net2 vom2 vdd vdd sky130_fd_pr__pfet_01v8 L=0.15 W=1 nf=1 ad='int((nf+1)/2) * W/nf * 0.29' as='int((nf+2)/2) * W/nf * 0.29'
+ pd='2*int((nf+1)/2) * (W/nf + 0.29)' ps='2*int((nf+2)/2) * (W/nf + 0.29)' nrd='0.29 / W' nrs='0.29 / W'
+ sa=0 sb=0 sd=0 mult=1 m=1
XM24 net2 vom2 vss vss sky130_fd_pr__nfet_01v8 L=0.15 W=0.5 nf=1 ad='int((nf+1)/2) * W/nf * 0.29' as='int((nf+2)/2) * W/nf * 0.29'
+ pd='2*int((nf+1)/2) * (W/nf + 0.29)' ps='2*int((nf+2)/2) * (W/nf + 0.29)' nrd='0.29 / W' nrs='0.29 / W'
+ sa=0 sb=0 sd=0 mult=1 m=1
XM15 net5 vop2 net3 vdd sky130_fd_pr__pfet_01v8_lvt L=0.4 W=5 nf=1 ad='int((nf+1)/2) * W/nf * 0.29' as='int((nf+2)/2) * W/nf * 0.29'
+ pd='2*int((nf+1)/2) * (W/nf + 0.29)' ps='2*int((nf+2)/2) * (W/nf + 0.29)' nrd='0.29 / W' nrs='0.29 / W'
+ sa=0 sb=0 sd=0 mult=1 m=1
XM16 net6 vom2 net4 vdd sky130_fd_pr__pfet_01v8_lvt L=0.4 W=5 nf=1 ad='int((nf+1)/2) * W/nf * 0.29' as='int((nf+2)/2) * W/nf * 0.29'
+ pd='2*int((nf+1)/2) * (W/nf + 0.29)' ps='2*int((nf+2)/2) * (W/nf + 0.29)' nrd='0.29 / W' nrs='0.29 / W'
+ sa=0 sb=0 sd=0 mult=1 m=1
XM25 net5 latch vom2 vss sky130_fd_pr__nfet_01v8_lvt L=0.15 W=1 nf=1 ad='int((nf+1)/2) * W/nf * 0.29'
+ as='int((nf+2)/2) * W/nf * 0.29' pd='2*int((nf+1)/2) * (W/nf + 0.29)' ps='2*int((nf+2)/2) * (W/nf + 0.29)'
+ nrd='0.29 / W' nrs='0.29 / W' sa=0 sb=0 sd=0 mult=1 m=1
XM26 net6 latch vop2 vss sky130_fd_pr__nfet_01v8_lvt L=0.15 W=1 nf=1 ad='int((nf+1)/2) * W/nf * 0.29'
+ as='int((nf+2)/2) * W/nf * 0.29' pd='2*int((nf+1)/2) * (W/nf + 0.29)' ps='2*int((nf+2)/2) * (W/nf + 0.29)'
+ nrd='0.29 / W' nrs='0.29 / W' sa=0 sb=0 sd=0 mult=1 m=1
x30 latch vss vss vdd vdd latch_n sky130_fd_sc_hd__inv_1
XM27 vss ibn_1u vss vss sky130_fd_pr__nfet_01v8 L=20 W=3 nf=1 ad='int((nf+1)/2) * W/nf * 0.29' as='int((nf+2)/2) * W/nf * 0.29'
+ pd='2*int((nf+1)/2) * (W/nf + 0.29)' ps='2*int((nf+2)/2) * (W/nf + 0.29)' nrd='0.29 / W' nrs='0.29 / W'
+ sa=0 sb=0 sd=0 mult=2 m=2
XM28 vss vss vss vss sky130_fd_pr__nfet_01v8_lvt L=1 W=2 nf=1 ad='int((nf+1)/2) * W/nf * 0.29' as='int((nf+2)/2) * W/nf * 0.29'
+ pd='2*int((nf+1)/2) * (W/nf + 0.29)' ps='2*int((nf+2)/2) * (W/nf + 0.29)' nrd='0.29 / W' nrs='0.29 / W'
+ sa=0 sb=0 sd=0 mult=2 m=2
XM29 vss vss vss vss sky130_fd_pr__nfet_01v8_lvt L=1 W=1 nf=1 ad='int((nf+1)/2) * W/nf * 0.29' as='int((nf+2)/2) * W/nf * 0.29'
+ pd='2*int((nf+1)/2) * (W/nf + 0.29)' ps='2*int((nf+2)/2) * (W/nf + 0.29)' nrd='0.29 / W' nrs='0.29 / W'
+ sa=0 sb=0 sd=0 mult=20 m=20
XM30 vdd vbp vdd vdd sky130_fd_pr__pfet_01v8_lvt L=5 W=5 nf=1 ad='int((nf+1)/2) * W/nf * 0.29' as='int((nf+2)/2) * W/nf * 0.29'
+ pd='2*int((nf+1)/2) * (W/nf + 0.29)' ps='2*int((nf+2)/2) * (W/nf + 0.29)' nrd='0.29 / W' nrs='0.29 / W'
+ sa=0 sb=0 sd=0 mult=2 m=2
XM31 vdd vdd vdd vdd sky130_fd_pr__pfet_01v8_lvt L=1 W=5 nf=1 ad='int((nf+1)/2) * W/nf * 0.29' as='int((nf+2)/2) * W/nf * 0.29'
+ pd='2*int((nf+1)/2) * (W/nf + 0.29)' ps='2*int((nf+2)/2) * (W/nf + 0.29)' nrd='0.29 / W' nrs='0.29 / W'
+ sa=0 sb=0 sd=0 mult=2 m=2
.ends

.GLOBAL GND
.end
